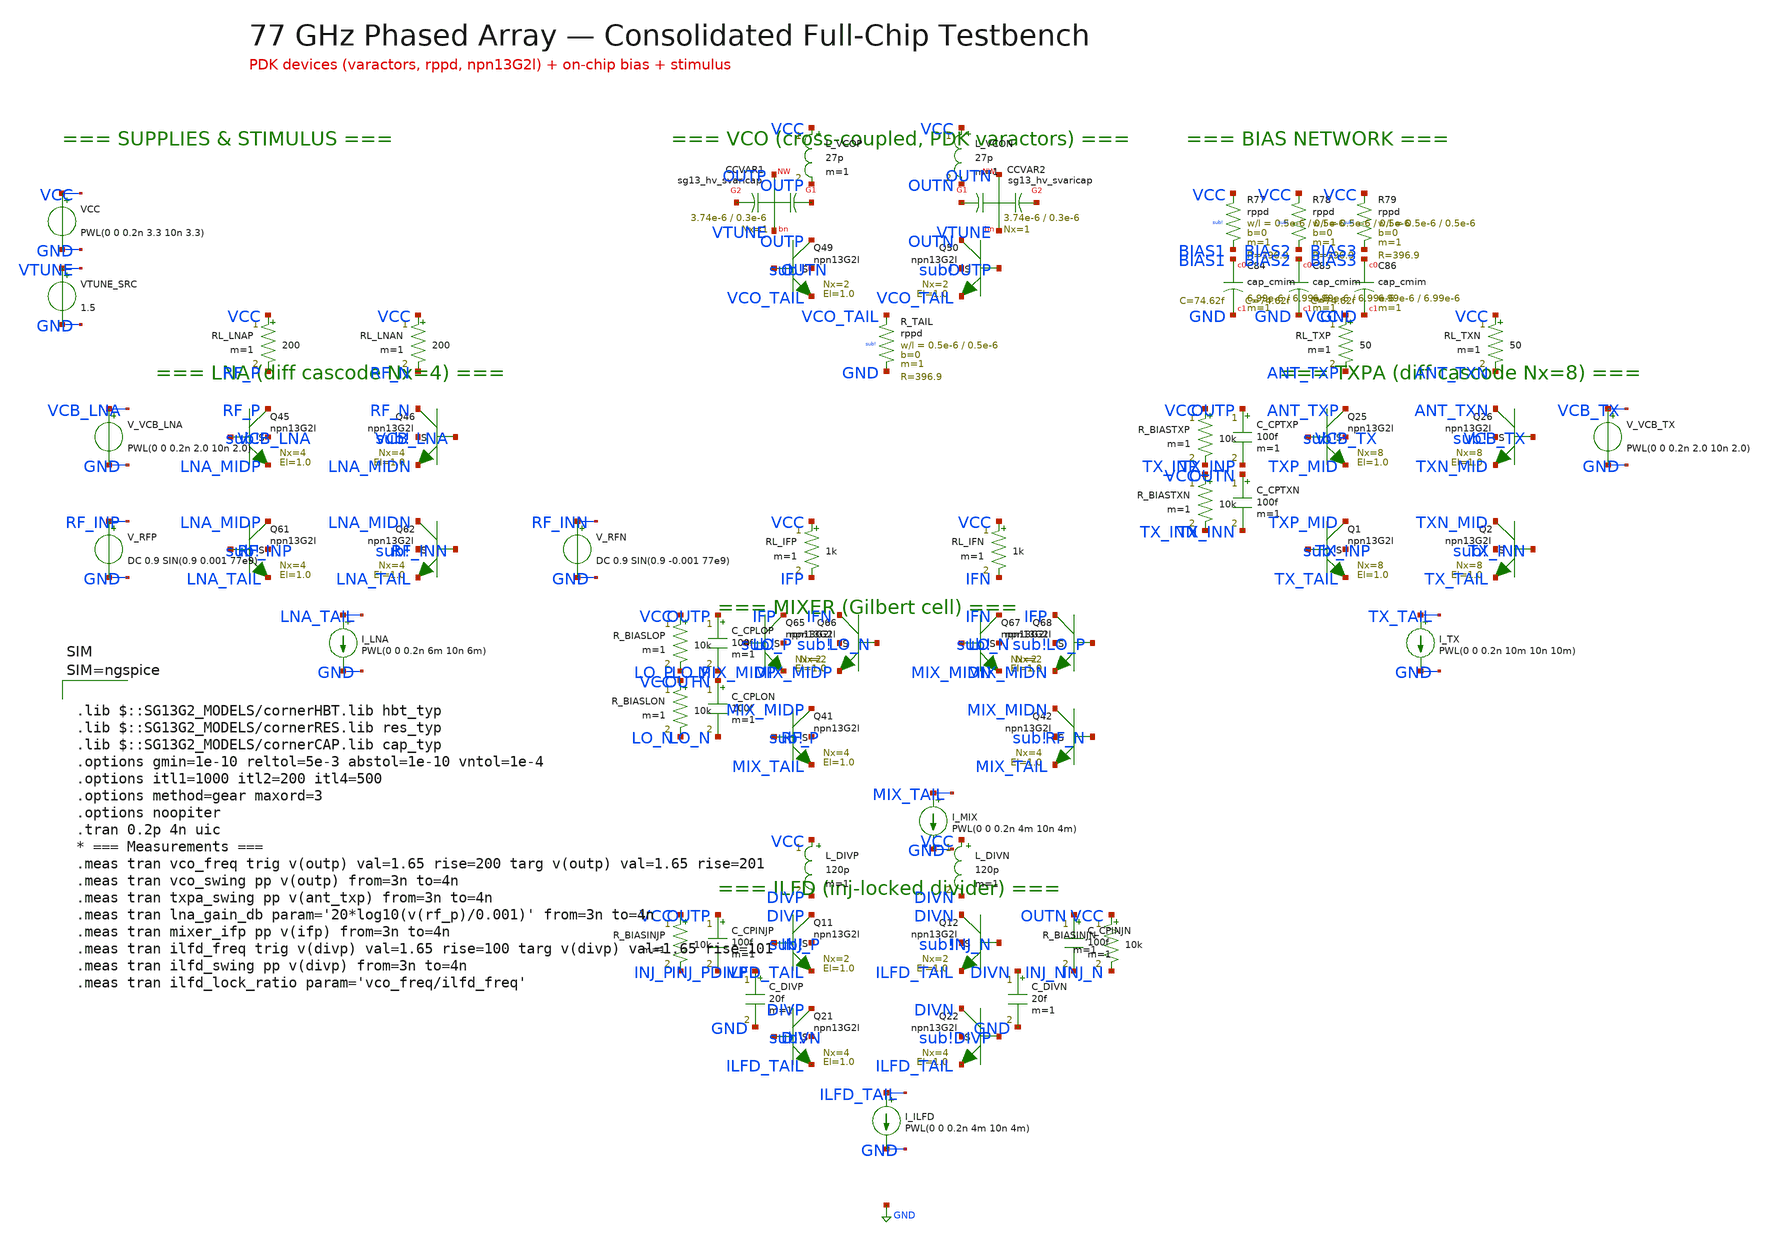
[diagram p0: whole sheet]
** sch_path: layout/testbenches/tb_fullchip_consolidated.sch
**.subckt tb_fullchip_consolidated
XQ49 OUTP OUTN VCO_TAIL sub! npn13G2l Nx=2 El=1.0 mm_ok=1
XQ50 OUTN OUTP VCO_TAIL sub! npn13G2l Nx=2 El=1.0 mm_ok=1
XCVAR1 net1 OUTP net2 VTUNE sg13_hv_svaricap w=3.74e-6 l=0.3e-6 Nx=1
XCVAR2 net3 OUTN net4 VTUNE sg13_hv_svaricap w=3.74e-6 l=0.3e-6 Nx=1
XR_TAIL VCO_TAIL GND sub! rppd w=0.5e-6 l=0.5e-6 m=1 b=0 mm_ok=1
L_VCOP VCC OUTP 27p m=1
L_VCON VCC OUTN 27p m=1
XQ1 TXP_MID TX_INP TX_TAIL sub! npn13G2l Nx=8 El=1.0 mm_ok=1
XQ2 TXN_MID TX_INN TX_TAIL sub! npn13G2l Nx=8 El=1.0 mm_ok=1
XQ25 ANT_TXP VCB_TX TXP_MID sub! npn13G2l Nx=8 El=1.0 mm_ok=1
XQ26 ANT_TXN VCB_TX TXN_MID sub! npn13G2l Nx=8 El=1.0 mm_ok=1
RL_TXP VCC ANT_TXP 50 m=1
RL_TXN VCC ANT_TXN 50 m=1
C_CPTXP OUTP TX_INP 100f m=1
C_CPTXN OUTN TX_INN 100f m=1
R_BIASTXP VCC TX_INP 10k m=1
R_BIASTXN VCC TX_INN 10k m=1
I_TX TX_TAIL GND PWL(0 0 0.2n 10m 10n 10m)
V_VCB_TX VCB_TX GND PWL(0 0 0.2n 2.0 10n 2.0)
XQ61 LNA_MIDP RF_INP LNA_TAIL sub! npn13G2l Nx=4 El=1.0 mm_ok=1
XQ62 LNA_MIDN RF_INN LNA_TAIL sub! npn13G2l Nx=4 El=1.0 mm_ok=1
XQ45 RF_P VCB_LNA LNA_MIDP sub! npn13G2l Nx=4 El=1.0 mm_ok=1
XQ46 RF_N VCB_LNA LNA_MIDN sub! npn13G2l Nx=4 El=1.0 mm_ok=1
RL_LNAP VCC RF_P 200 m=1
RL_LNAN VCC RF_N 200 m=1
I_LNA LNA_TAIL GND PWL(0 0 0.2n 6m 10n 6m)
V_VCB_LNA VCB_LNA GND PWL(0 0 0.2n 2.0 10n 2.0)
V_RFP RF_INP GND DC 0.9 SIN(0.9 0.001 77e9)
V_RFN RF_INN GND DC 0.9 SIN(0.9 -0.001 77e9)
XQ41 MIX_MIDP RF_P MIX_TAIL sub! npn13G2l Nx=4 El=1.0 mm_ok=1
XQ42 MIX_MIDN RF_N MIX_TAIL sub! npn13G2l Nx=4 El=1.0 mm_ok=1
XQ65 IFP LO_P MIX_MIDP sub! npn13G2l Nx=2 El=1.0 mm_ok=1
XQ66 IFN LO_N MIX_MIDP sub! npn13G2l Nx=2 El=1.0 mm_ok=1
XQ67 IFN LO_N MIX_MIDN sub! npn13G2l Nx=2 El=1.0 mm_ok=1
XQ68 IFP LO_P MIX_MIDN sub! npn13G2l Nx=2 El=1.0 mm_ok=1
RL_IFP VCC IFP 1k m=1
RL_IFN VCC IFN 1k m=1
C_CPLOP OUTP LO_P 100f m=1
C_CPLON OUTN LO_N 100f m=1
R_BIASLOP VCC LO_P 10k m=1
R_BIASLON VCC LO_N 10k m=1
I_MIX MIX_TAIL GND PWL(0 0 0.2n 4m 10n 4m)
XQ21 DIVP DIVN ILFD_TAIL sub! npn13G2l Nx=4 El=1.0 mm_ok=1
XQ22 DIVN DIVP ILFD_TAIL sub! npn13G2l Nx=4 El=1.0 mm_ok=1
XQ11 DIVP INJ_P ILFD_TAIL sub! npn13G2l Nx=2 El=1.0 mm_ok=1
XQ12 DIVN INJ_N ILFD_TAIL sub! npn13G2l Nx=2 El=1.0 mm_ok=1
L_DIVP VCC DIVP 120p m=1
L_DIVN VCC DIVN 120p m=1
C_DIVP DIVP GND 20f m=1
C_DIVN DIVN GND 20f m=1
C_CPINJP OUTP INJ_P 100f m=1
C_CPINJN OUTN INJ_N 100f m=1
R_BIASINJP VCC INJ_P 10k m=1
R_BIASINJN VCC INJ_N 10k m=1
I_ILFD ILFD_TAIL GND PWL(0 0 0.2n 4m 10n 4m)
VCC VCC GND PWL(0 0 0.2n 3.3 10n 3.3)
VTUNE_SRC VTUNE GND 1.5
XR77 VCC BIAS1 sub! rppd w=0.5e-6 l=0.5e-6 m=1 b=0 mm_ok=1
XR78 VCC BIAS2 sub! rppd w=0.5e-6 l=0.5e-6 m=1 b=0 mm_ok=1
XR79 VCC BIAS3 sub! rppd w=0.5e-6 l=0.5e-6 m=1 b=0 mm_ok=1
XC84 BIAS1 GND cap_cmim w=6.99e-6 l=6.99e-6 m=1 mm_ok=1
XC85 BIAS2 GND cap_cmim w=6.99e-6 l=6.99e-6 m=1 mm_ok=1
XC86 BIAS3 GND cap_cmim w=6.99e-6 l=6.99e-6 m=1 mm_ok=1
**** begin user architecture code



.lib $::SG13G2_MODELS/cornerHBT.lib hbt_typ
.lib $::SG13G2_MODELS/cornerRES.lib res_typ
.lib $::SG13G2_MODELS/cornerCAP.lib cap_typ
.options gmin=1e-10 reltol=5e-3 abstol=1e-10 vntol=1e-4
.options itl1=1000 itl2=200 itl4=500
.options method=gear maxord=3
.options noopiter
.tran 0.2p 4n uic
* === Measurements ===
.meas tran vco_freq trig v(outp) val=1.65 rise=200 targ v(outp) val=1.65 rise=201
.meas tran vco_swing pp v(outp) from=3n to=4n
.meas tran txpa_swing pp v(ant_txp) from=3n to=4n
.meas tran lna_gain_db param='20*log10(v(rf_p)/0.001)' from=3n to=4n
.meas tran mixer_ifp pp v(ifp) from=3n to=4n
.meas tran ilfd_freq trig v(divp) val=1.65 rise=100 targ v(divp) val=1.65 rise=101
.meas tran ilfd_swing pp v(divp) from=3n to=4n
.meas tran ilfd_lock_ratio param='vco_freq/ilfd_freq'



**** end user architecture code
**.ends
.GLOBAL GND
.end
